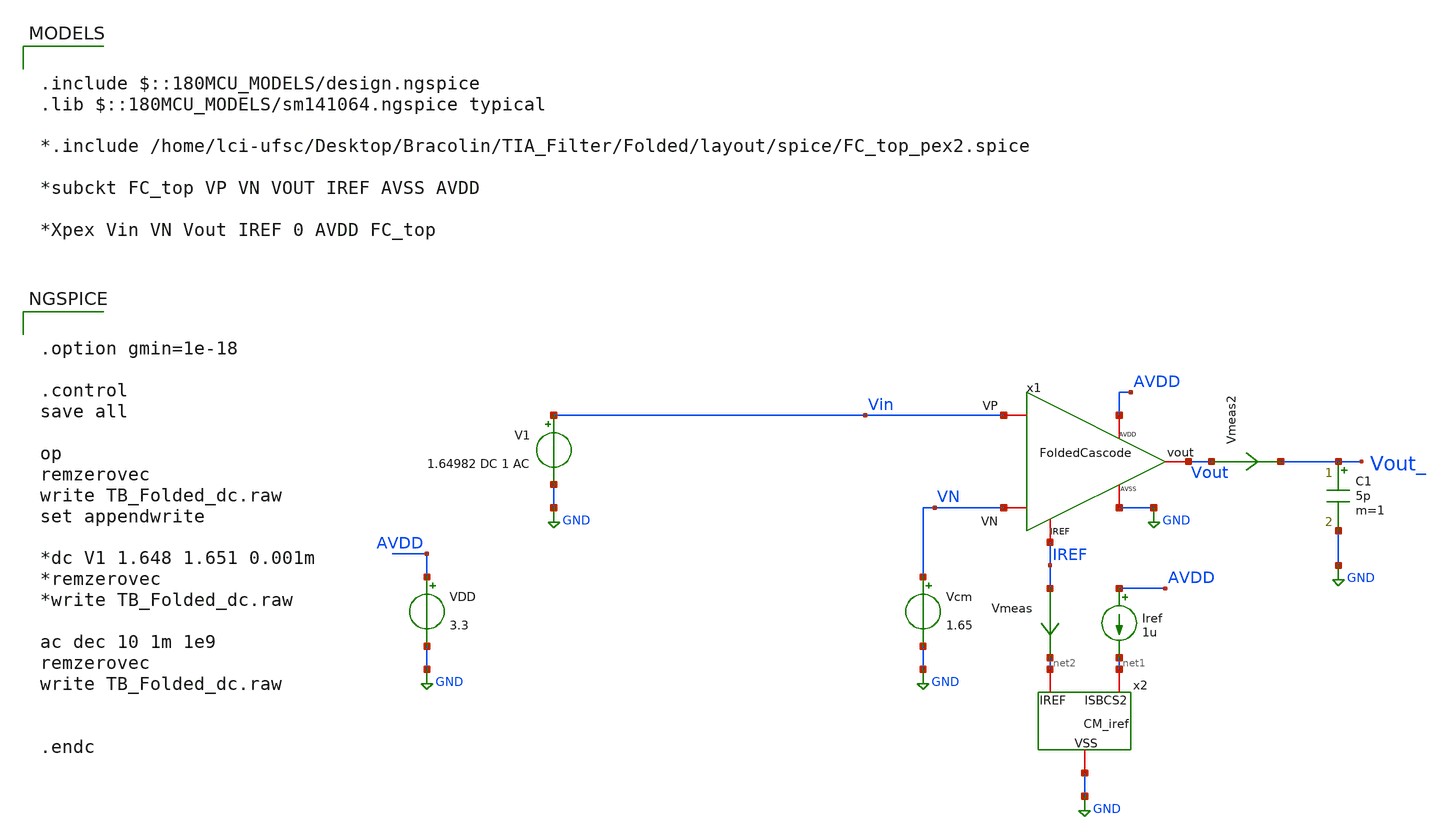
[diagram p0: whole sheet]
** sch_path: TIA_Filter/Folded/TB_Folded_dc.sch
**.subckt TB_Folded_dc
VDD AVDD GND 3.3
Iref AVDD net1 1u
Vcm VN GND 1.65
Vmeas2 Vout Vout_ 0
.save i(vmeas2)
C1 Vout_ GND 5p m=1
x1 Vin VN Vout IREF AVDD GND FoldedCascode
V1 Vin GND 1.64982 DC 1 AC
x2 net1 net2 GND CM_iref
Vmeas IREF net2 0
.save i(vmeas)
**** begin user architecture code

.include $::180MCU_MODELS/design.ngspice
.lib $::180MCU_MODELS/sm141064.ngspice typical

*.include /home/lci-ufsc/Desktop/Bracolin/TIA_Filter/Folded/layout/spice/FC_top_pex2.spice

*subckt FC_top VP VN VOUT IREF AVSS AVDD

*Xpex Vin VN Vout IREF 0 AVDD FC_top



.option gmin=1e-18

.control
save all

op
remzerovec
write TB_Folded_dc.raw
set appendwrite

*dc V1 1.648 1.651 0.001m
*remzerovec
*write TB_Folded_dc.raw

ac dec 10 1m 1e9
remzerovec
write TB_Folded_dc.raw


.endc


**** end user architecture code
**.ends
.GLOBAL GND
.end
